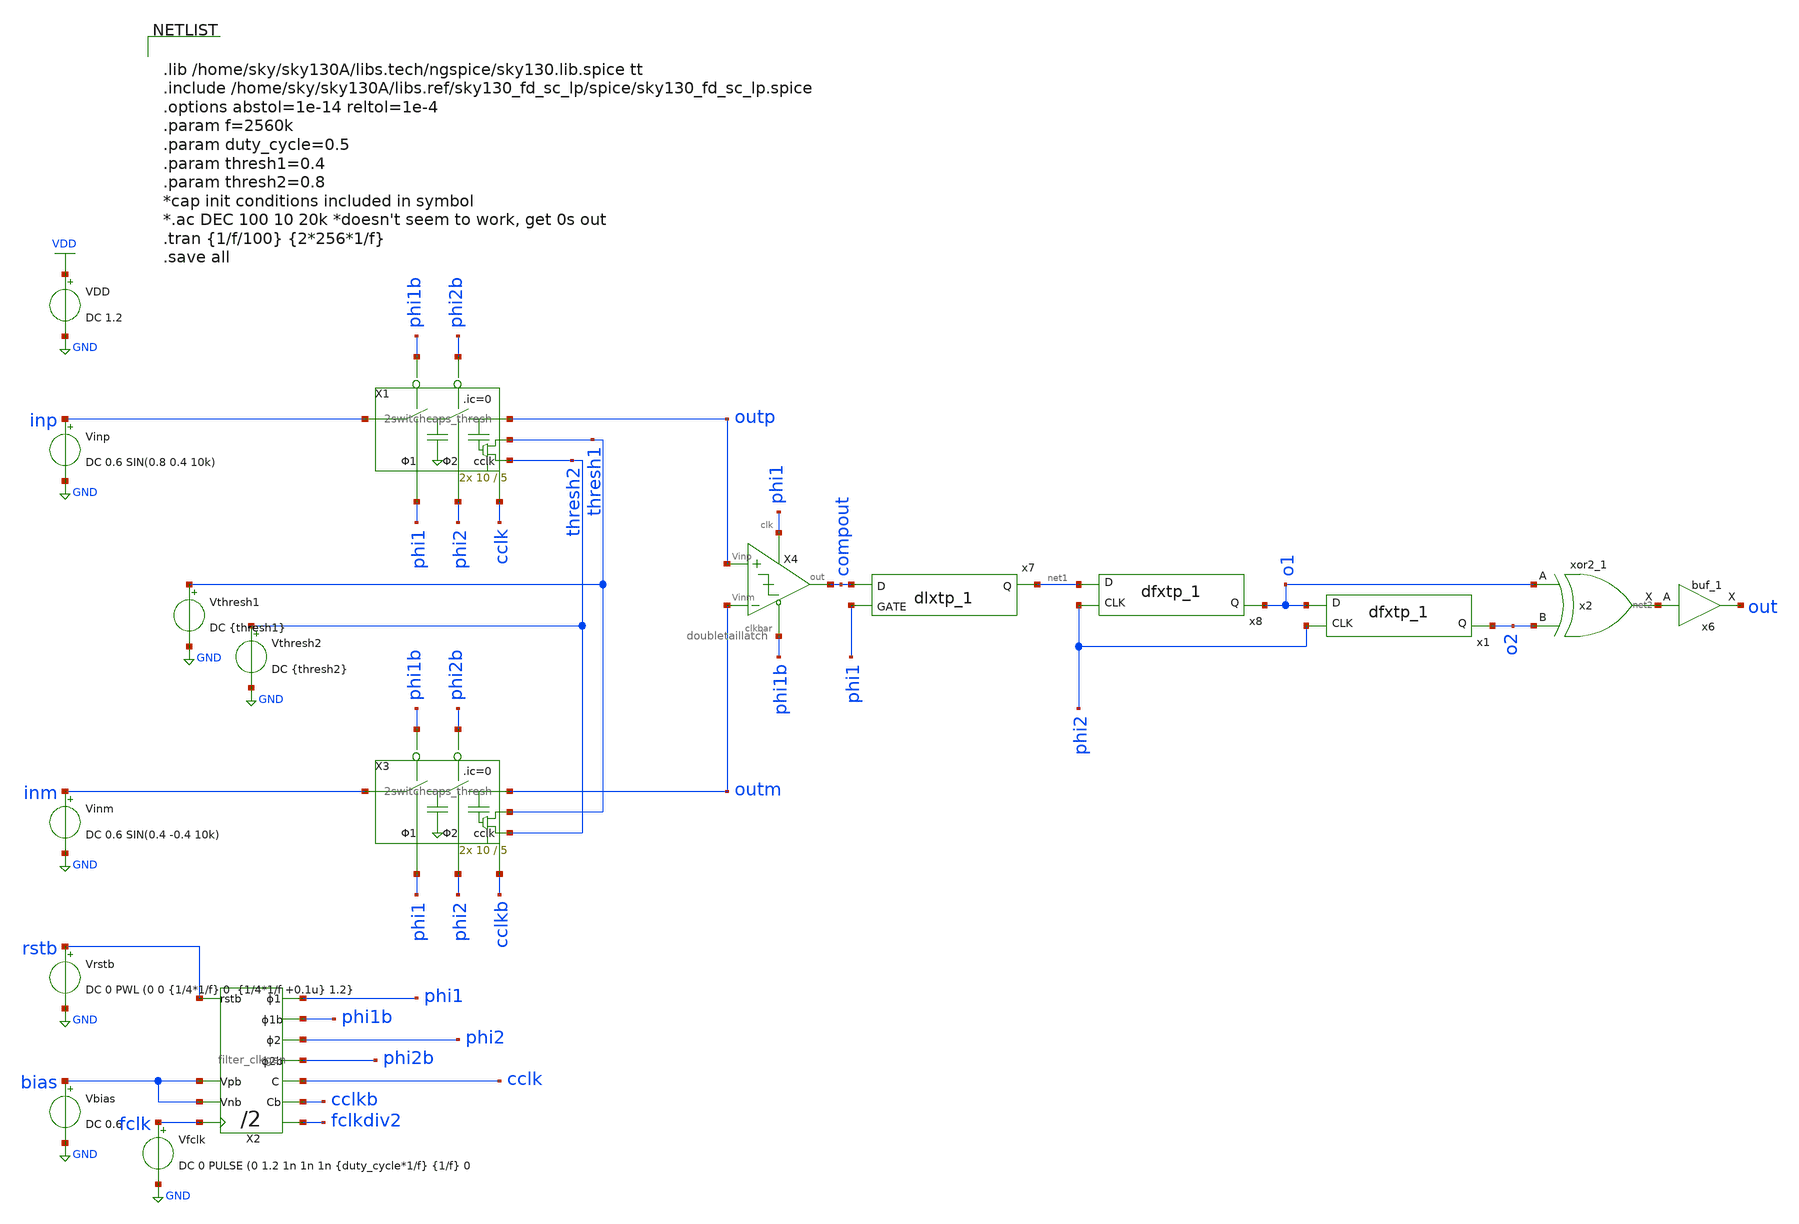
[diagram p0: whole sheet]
** sch_path: xschem/Switched_Caps/2switchcaps_thresh_diff_tb.sch
**.subckt 2switchcaps_thresh_diff_tb
Vinp inp GND DC 0.6 SIN(0.8 0.4 10k)
VDD VDD GND DC 1.2
Vfclk fclk GND DC 0 PULSE (0 1.2 1n 1n 1n {duty_cycle*1/f} {1/f} 0
X1 inp outp phi2 phi1 phi1b phi2b thresh2 cclk thresh1 2switchcaps_thresh Wcap=10 Lcap=5
X2 rstb fclk phi2b phi2 phi1b phi1 cclkb cclk fclkdiv2 bias bias filter_clkgen
Vbias bias GND DC 0.6
Vthresh1 thresh1 GND DC {thresh1}
Vthresh2 thresh2 GND DC {thresh2}
Vrstb rstb GND DC 0 PWL (0 0 {1/4*1/f} 0 {1/4*1/f +0.1u} 1.2}
Vinm inm GND DC 0.6 SIN(0.4 -0.4 10k)
X3 inm outm phi2 phi1 phi1b phi2b thresh2 cclkb thresh1 2switchcaps_thresh Wcap=10 Lcap=5
X4 outp outm compout phi1 phi1b doubletaillatch
x2 o1 o2 GND GND VDD VDD net2 sky130_fd_sc_lp__xor2_1
x6 net2 GND GND VDD VDD out sky130_fd_sc_lp__buf_1
x7 compout phi1 gnd gnd vdd vdd net1 sky130_fd_sc_lp__dlxtp_1
x8 phi2 net1 gnd gnd vdd vdd o1 sky130_fd_sc_lp__dfxtp_1
x1 phi2 o1 gnd gnd vdd vdd o2 sky130_fd_sc_lp__dfxtp_1
**** begin user architecture code


.lib /home/sky/sky130A/libs.tech/ngspice/sky130.lib.spice tt
.include /home/sky/sky130A/libs.ref/sky130_fd_sc_lp/spice/sky130_fd_sc_lp.spice
.options abstol=1e-14 reltol=1e-4
.param f=2560k
.param duty_cycle=0.5
.param thresh1=0.4
.param thresh2=0.8
*cap init conditions included in symbol
*.ac DEC 100 10 20k *doesn't seem to work, get 0s out
.tran {1/f/100} {2*256*1/f}
.save all


**** end user architecture code
**.ends
.GLOBAL GND
.GLOBAL VDD
.end
